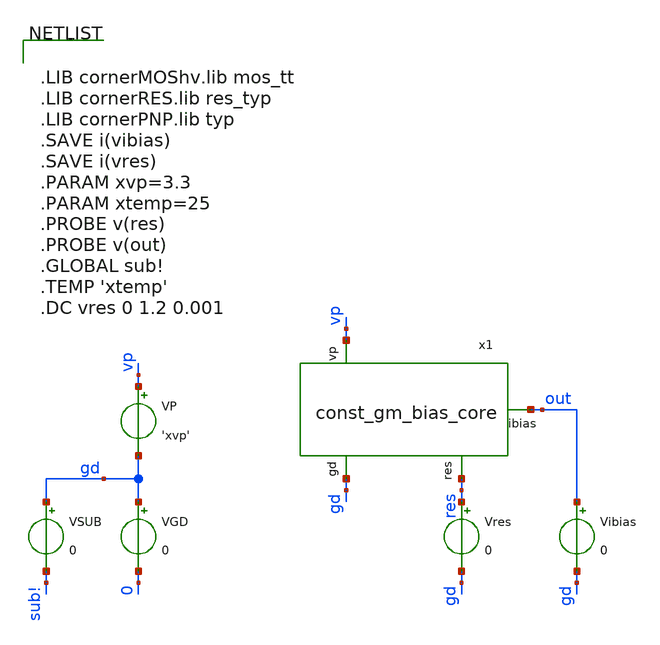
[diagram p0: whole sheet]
** sch_path: testbench/const_gm_bias_tune_tb.sch
**.subckt const_gm_bias_tune_tb
x1 vp out gd res const_gm_bias_core
VP vp gd 'xvp'
.save i(vp)
VGD gd 0 0
VSUB gd sub! 0
Vres res gd 0
.save i(vres)
Vibias out gd 0
.save i(vibias)
**** begin user architecture code


.LIB cornerMOShv.lib mos_tt
.LIB cornerRES.lib res_typ
.LIB cornerPNP.lib typ
.SAVE i(vibias)
.SAVE i(vres)
.PARAM xvp=3.3
.PARAM xtemp=25
.PROBE v(res)
.PROBE v(out)
.GLOBAL sub!
.TEMP 'xtemp'
.DC vres 0 1.2 0.001


**** end user architecture code
**.ends

* expanding   symbol:  /foss/designs/test/circuit/const_gm_bias_core.sym # of pins=4
** sym_path: circuit/const_gm_bias_core.sym
** sch_path: circuit/const_gm_bias_core.sch
.subckt const_gm_bias_core vp ibias gd res
*.ipin vp
*.ipin gd
*.opin ibias
*.opin res
XM1 nbias nbias gd gd sg13_hv_nmos w=0.6u l=2u ng=1 m=2 mm_ok=1
XM2 pbias nbias res gd sg13_hv_nmos w=0.6u l=2u ng=1 m=4 mm_ok=1
XM4 pbias pbias vp vp sg13_hv_pmos w=0.6u l=2u ng=1 m=2 mm_ok=1
XM3 nbias pbias vp vp sg13_hv_pmos w=0.6u l=2u ng=1 m=2 mm_ok=1
XM5 ibias pbias vp vp sg13_hv_pmos w=0.6u l=2u ng=1 m=2 mm_ok=1
XM7 stup gd vp vp sg13_hv_pmos w=0.6u l=4u ng=1 m=1 mm_ok=1
XM6 stup nbias gd gd sg13_hv_nmos w=0.6u l=2u ng=1 m=4 mm_ok=1
XM8 pbias stup gd gd sg13_hv_nmos w=0.6u l=2u ng=1 m=2 mm_ok=1
.ends

.end
